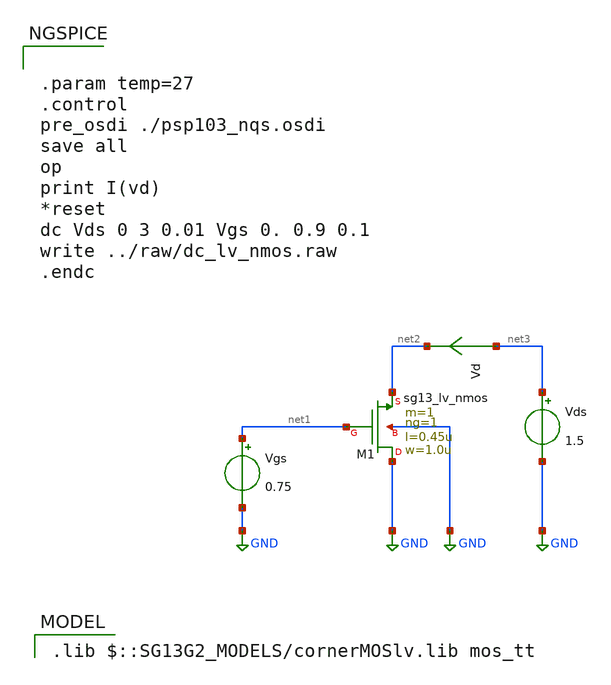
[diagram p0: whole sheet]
** sch_path: ihp-sg13g2/libs.tech/xschem/sg13g2_tests/dc_lv_nmos.sch
* Copyright 2023 IHP PDK Authors
**.subckt dc_lv_nmos
Vgs net1 GND 0.75
Vds net3 GND 1.5
XM1 GND net1 net2 GND sg13_lv_nmos w=1.0u l=0.45u ng=1 m=1 mm_ok=1
Vd net3 net2 0
.save i(vd)
**** begin user architecture code
 .lib $::SG13G2_MODELS/cornerMOSlv.lib mos_tt



.param temp=27
.control
pre_osdi ./psp103_nqs.osdi
save all
op
print I(vd)
*reset
dc Vds 0 3 0.01 Vgs 0. 0.9 0.1
write ../raw/dc_lv_nmos.raw
.endc


**** end user architecture code
**.ends
.GLOBAL GND
.end
